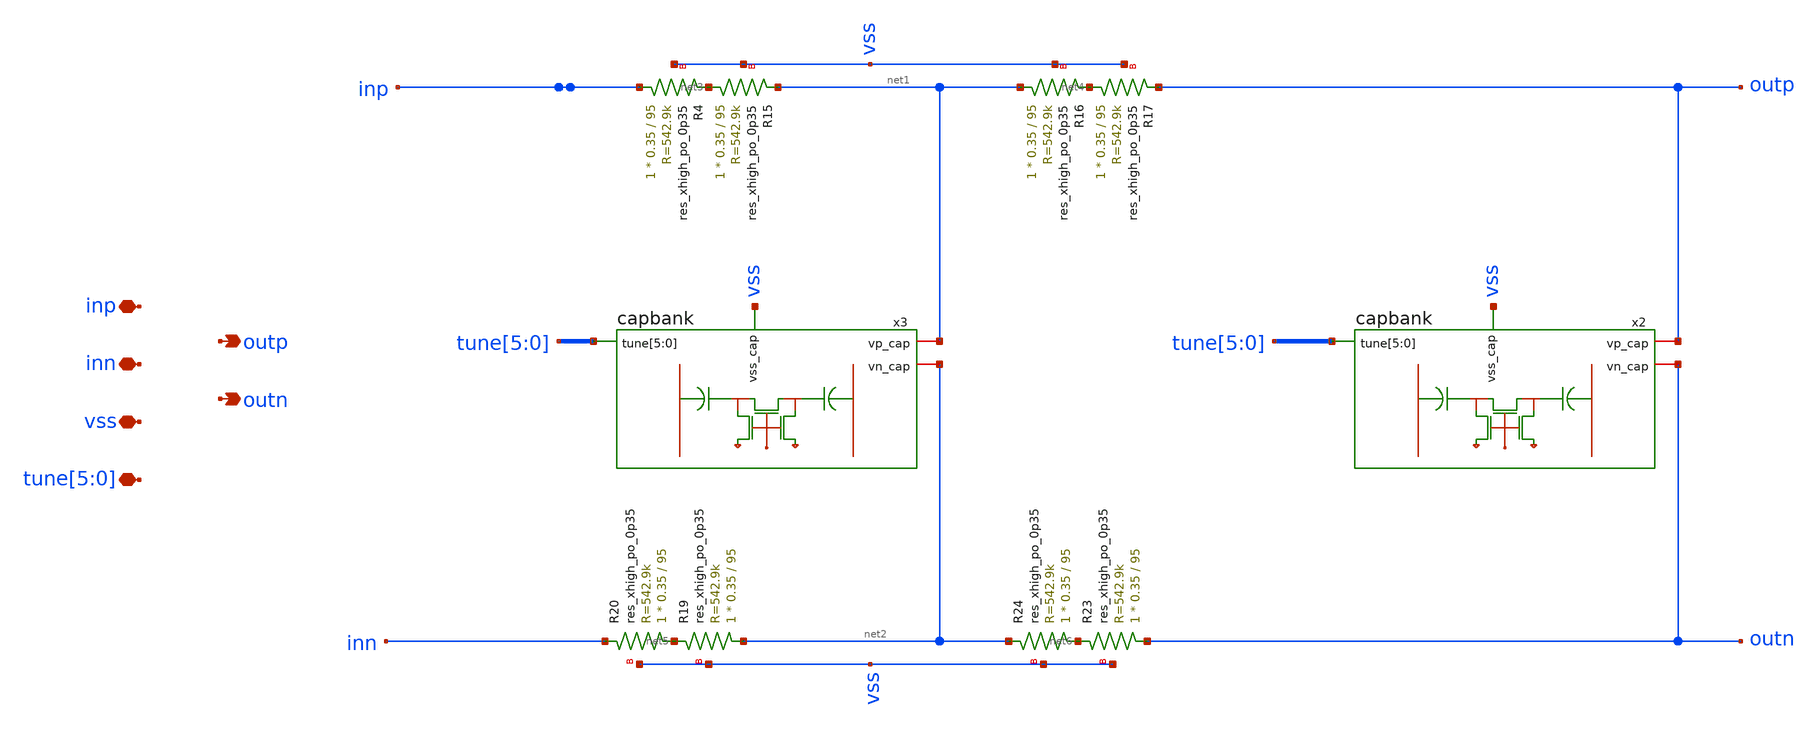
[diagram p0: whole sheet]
** sch_path: AAFilter.sch
**.subckt AAFilter inp inn vss outp outn tune[5],tune[4],tune[3],tune[2],tune[1],tune[0]
*.iopin inp
*.iopin inn
*.iopin vss
*.opin outp
*.opin outn
*.iopin tune[5],tune[4],tune[3],tune[2],tune[1],tune[0]
XR4 inp net3 vss sky130_fd_pr__res_xhigh_po_0p35 L=95 mult=1 m=1
XR15 net3 net1 vss sky130_fd_pr__res_xhigh_po_0p35 L=95 mult=1 m=1
XR16 net1 net4 vss sky130_fd_pr__res_xhigh_po_0p35 L=95 mult=1 m=1
XR17 net4 outp vss sky130_fd_pr__res_xhigh_po_0p35 L=95 mult=1 m=1
XR19 net2 net5 vss sky130_fd_pr__res_xhigh_po_0p35 L=95 mult=1 m=1
XR20 net5 inn vss sky130_fd_pr__res_xhigh_po_0p35 L=95 mult=1 m=1
XR23 outn net6 vss sky130_fd_pr__res_xhigh_po_0p35 L=95 mult=1 m=1
XR24 net6 net2 vss sky130_fd_pr__res_xhigh_po_0p35 L=95 mult=1 m=1
x2 outp outn vss tune[5] tune[4] tune[3] tune[2] tune[1] tune[0] capbank
x3 net1 net2 vss tune[5] tune[4] tune[3] tune[2] tune[1] tune[0] capbank
**.ends

* expanding   symbol:  LNA/capbank.sym # of pins=4
** sym_path: capbank.sym
** sch_path: capbank.sch
.subckt capbank vp_cap vn_cap vss_cap tune[5] tune[4] tune[3] tune[2] tune[1] tune[0]
*.iopin vp_cap
*.iopin vn_cap
*.ipin tune[5],tune[4],tune[3],tune[2],tune[1],tune[0]
*.ipin vss_cap
x6 tune[5] net1 net2 vss_cap cap_sw
XC11 net2 vp_cap sky130_fd_pr__cap_mim_m3_1 W=5 L=5.5 MF=160 m=160
XC12 net1 vn_cap sky130_fd_pr__cap_mim_m3_1 W=5 L=5.5 MF=160 m=160
XC21 vn_cap net1 sky130_fd_pr__cap_mim_m3_1 W=5 L=5.5 MF=160 m=160
XC22 vp_cap net2 sky130_fd_pr__cap_mim_m3_1 W=5 L=5.5 MF=160 m=160
x1 tune[4] net3 net4 vss_cap cap_sw
XC1 net4 vp_cap sky130_fd_pr__cap_mim_m3_1 W=5 L=5.5 MF=80 m=80
XC2 net3 vn_cap sky130_fd_pr__cap_mim_m3_1 W=5 L=5.5 MF=80 m=80
XC3 vn_cap net3 sky130_fd_pr__cap_mim_m3_1 W=5 L=5.5 MF=80 m=80
XC4 vp_cap net4 sky130_fd_pr__cap_mim_m3_1 W=5 L=5.5 MF=80 m=80
x2 tune[3] net5 net6 vss_cap cap_sw
XC5 net6 vp_cap sky130_fd_pr__cap_mim_m3_1 W=5 L=5.5 MF=40 m=40
XC6 net5 vn_cap sky130_fd_pr__cap_mim_m3_1 W=5 L=5.5 MF=40 m=40
XC7 vn_cap net5 sky130_fd_pr__cap_mim_m3_1 W=5 L=5.5 MF=40 m=40
XC8 vp_cap net6 sky130_fd_pr__cap_mim_m3_1 W=5 L=5.5 MF=40 m=40
x3 tune[2] net7 net8 vss_cap cap_sw
XC9 net8 vp_cap sky130_fd_pr__cap_mim_m3_1 W=5 L=5.5 MF=20 m=20
XC10 net7 vn_cap sky130_fd_pr__cap_mim_m3_1 W=5 L=5.5 MF=20 m=20
XC13 vn_cap net7 sky130_fd_pr__cap_mim_m3_1 W=5 L=5.5 MF=20 m=20
XC14 vp_cap net8 sky130_fd_pr__cap_mim_m3_1 W=5 L=5.5 MF=20 m=20
x4 tune[1] net9 net10 vss_cap cap_sw
XC15 net10 vp_cap sky130_fd_pr__cap_mim_m3_1 W=5 L=5.5 MF=10 m=10
XC16 net9 vn_cap sky130_fd_pr__cap_mim_m3_1 W=5 L=5.5 MF=10 m=10
XC17 vn_cap net9 sky130_fd_pr__cap_mim_m3_1 W=5 L=5.5 MF=10 m=10
XC18 vp_cap net10 sky130_fd_pr__cap_mim_m3_1 W=5 L=5.5 MF=10 m=10
x5 tune[0] net11 net12 vss_cap cap_sw
XC19 vp_cap net12 sky130_fd_pr__cap_mim_m3_1 W=5 L=5.5 MF=5 m=5
XC20 vn_cap net11 sky130_fd_pr__cap_mim_m3_1 W=5 L=5.5 MF=5 m=5
XC23 vn_cap net11 sky130_fd_pr__cap_mim_m3_1 W=5 L=5.5 MF=5 m=5
XC24 vp_cap net12 sky130_fd_pr__cap_mim_m3_1 W=5 L=5.5 MF=5 m=5
.ends


* expanding   symbol:  LNA/cap_sw.sym # of pins=4
** sym_path: cap_sw.sym
** sch_path: cap_sw.sch
.subckt cap_sw en_sw vn_sw vp_sw vss_sw
*.ipin en_sw
*.ipin vss_sw
*.opin vn_sw
*.opin vp_sw
XM15 vp_sw en_sw vn_sw vss_sw sky130_fd_pr__nfet_01v8 L=0.15 W='5 * 13 ' nf=13 ad='int((nf+1)/2) * W / nf * 0.29'
+ as='int((nf+2)/2) * W / nf * 0.29' pd='2*int((nf+1)/2) * (W / nf + 0.29)' ps='2*int((nf+2)/2) * (W / nf + 0.29)'
+ nrd='0.29 / W ' nrs='0.29 / W ' sa=0 sb=0 sd=0 mult=1 m=1
XM5 vn_sw en_sw vss_sw vss_sw sky130_fd_pr__nfet_01v8 L=0.15 W='5 * 1 ' nf=1 ad='int((nf+1)/2) * W / nf * 0.29'
+ as='int((nf+2)/2) * W / nf * 0.29' pd='2*int((nf+1)/2) * (W / nf + 0.29)' ps='2*int((nf+2)/2) * (W / nf + 0.29)'
+ nrd='0.29 / W ' nrs='0.29 / W ' sa=0 sb=0 sd=0 mult=1 m=1
XM7 vp_sw en_sw vss_sw vss_sw sky130_fd_pr__nfet_01v8 L=0.15 W='5 * 1 ' nf=1 ad='int((nf+1)/2) * W / nf * 0.29'
+ as='int((nf+2)/2) * W / nf * 0.29' pd='2*int((nf+1)/2) * (W / nf + 0.29)' ps='2*int((nf+2)/2) * (W / nf + 0.29)'
+ nrd='0.29 / W ' nrs='0.29 / W ' sa=0 sb=0 sd=0 mult=1 m=1
XM1 vss_sw vss_sw vss_sw vss_sw sky130_fd_pr__nfet_01v8 L=0.15 W='5 * 2 ' nf=2 ad='int((nf+1)/2) * W / nf * 0.29'
+ as='int((nf+2)/2) * W / nf * 0.29' pd='2*int((nf+1)/2) * (W / nf + 0.29)' ps='2*int((nf+2)/2) * (W / nf + 0.29)'
+ nrd='0.29 / W ' nrs='0.29 / W ' sa=0 sb=0 sd=0 mult=1 m=1
.ends

.end
